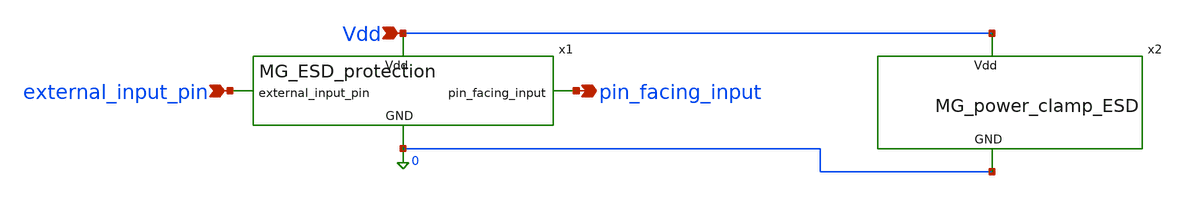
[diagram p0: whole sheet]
** sch_path: MG_ESD_protection/MG_ESD_protection_testbench.sch
**.subckt MG_ESD_protection_testbench external_input_pin Vdd pin_facing_input
*.ipin external_input_pin
*.ipin Vdd
*.opin pin_facing_input
x1 Vdd external_input_pin pin_facing_input 0 MG_ESD_protection
x2 Vdd 0 MG_power_clamp_ESD
**** begin user architecture code



.include /foss/pdks/gf180mcuD/libs.tech/ngspice/design.ngspice
.lib /foss/pdks/gf180mcuD/libs.tech/ngspice/sm141064.ngspice typical
.lib /foss/pdks/gf180mcuD/libs.tech/ngspice/sm141064.ngspice res_typical
.lib /foss/pdks/gf180mcuD/libs.tech/ngspice/sm141064.ngspice moscap_typical
.lib /foss/pdks/gf180mcuD/libs.tech/ngspice/sm141064.ngspice diode_typical
.lib /foss/pdks/gf180mcuD/libs.tech/ngspice/sm141064.ngspice mimcap_typical

* 1. Add ESD Current Source and Core Load Capacitor
* I_ESD injects the strike, and C_load represents the core receiver gate capacitance

I_ESD 0 external_input_pin PWL(0 0 1n 0)
C_load pin_facing_input 0 100f
Rleak Vdd 0 1G

* Add a controllable voltage source for Vdd (Assuming 3.3V - change to 5.0 if using 5V IOs)
* V_power Vdd 0 PWL(0 0)

.control

  * ==========================================
  * 3. HBM (Human Body Model) - 2kV Equivalent
  * Peak Current: ~1.33A, Rise: 5ns, Decay: ~150ns
  * ==========================================
  alter @I_ESD[pwl] = [ 0 0 5n 1.33 155n 0.49 305n 0.18 500n 0 ]



  * Run Transient Simulation (500ns duration, 1ns steps)
  tran 1n 1u

  * Extract Peak Voltages
  meas tran V_pad_max_HBM MAX v(external_input_pin)
  meas tran V_core_max_HBM MAX v(pin_facing_input)
  meas tran V_vdd_max_HBM MAX v(Vdd)

  * Print to Console
  print V_pad_max_HBM V_core_max_HBM


  * Plot HBM Waveforms
  plot v(external_input_pin) v(pin_facing_input) title 'HBM 2kV ESD Event' ylabel 'Voltage (V)' xlabel
+ 'Time (s)'
  plot v(pin_facing_input) title 'HBM 2kV ESD Event' ylabel 'Voltage (V)' xlabel 'Time (s)'
  plot v(Vdd) title 'HBM 2kV ESD Event' ylabel 'Vdd' xlabel 'Time'




* ==========================================
  * 3b. HBM - Power ON 1us after strike ends
  * Vdd ramps from 0V to 3.3V starting at 1.5us
  * ==========================================
*  alter @I_ESD[pwl] = [ 0 0 5n 1.33 155n 0.49 305n 0.18 500n 0 ]
*  alter @V_power[pwl] = [ 0 0 1.5u 0 1.6u 5 6u 5 ]

*  tran 0.1n 60u

*  meas tran V_pad_max_HBM_after MAX v(external_input_pin)
*  meas tran V_core_max_HBM_after MAX v(pin_facing_input)

*  print V_pad_max_HBM_after V_core_max_HBM_after
*  plot v(external_input_pin) v(pin_facing_input) title 'HBM (Power ON at 1.5us)' ylabel 'Voltage (V)'
*  plot v(Vdd) title 'HBM Vdd Supply (Delayed Power)' ylabel 'Vdd'

  * ==========================================
  * 3c. HBM - Powered ON during strike
  * Vdd is constant at 3.3V the entire time
  * ==========================================
*  alter @I_ESD[pwl] = [ 0 0 5n 1.33 155n 0.49 305n 0.18 500n 0 ]
*  alter @V_power[pwl] = [ 0 5 6u 5 ]

*  tran 0.1n 60u

*  meas tran V_pad_max_HBM_on MAX v(external_input_pin)
*  meas tran V_core_max_HBM_on MAX v(pin_facing_input)

*  print V_pad_max_HBM_on V_core_max_HBM_on
*  plot v(external_input_pin) v(pin_facing_input) title 'HBM (Already Powered ON)' ylabel 'Voltage (V)'

  * ==========================================
  * 4. CDM (Charged Device Model) - 500V Equivalent
  * Peak Current: ~5A, Rise: 250ps, Duration: ~2ns
  * ==========================================
  alter @I_ESD[pwl] = [ 0 0 250p 5.0 750p 0 1n -1.0 1.5n 0 3n 0 ]

  * Run Transient Simulation (3ns duration, 10ps steps)
  tran 10p 10n
  * Extract Peak Voltages
  meas tran V_pad_max_CDM MAX v(external_input_pin)
 meas tran V_core_max_CDM MAX v(pin_facing_input)
*  meas tran V_vdd_max_CDM MAX v(Vdd)

  * Print to Console
  print V_pad_max_CDM V_core_max_CDM


  * Plot CDM Waveforms
  plot v(external_input_pin) v(pin_facing_input) title 'CDM 500V ESD Event' ylabel 'Voltage (V)' xlabel
+ 'Time (s)'
  plot v(pin_facing_input) title 'CDM 500V ESD Event' ylabel 'Voltage (V)' xlabel 'Time (s)'
  plot v(Vdd) title 'CDM 500V ESD Event' ylabel 'Vdd' xlabel 'Time'

  * ==========================================
  * 4b. CDM - Power ON 1us after strike
  * Strike ends at 3ns. Vdd ramps to 3.3V starting at 1.003us
  * ==========================================
  * Reset V_power to default 0V before the run so earlier tests don't leak over
*  alter @V_power[pwl] = [ 0 0 1.003u 0 1.103u 5 6u 5 ]
*  alter @I_ESD[pwl] = [ 0 0 250p 5.0 750p 0 1n -1.0 1.5n 0 3n 0 ]

  * Note: 50p step used here to prevent massive file sizes over a 6us run
*  tran 50p 60u

*  meas tran V_pad_max_CDM_after MAX v(external_input_pin)
*  meas tran V_core_max_CDM_after MAX v(pin_facing_input)

*  print V_pad_max_CDM_after V_core_max_CDM_after
*  plot v(external_input_pin) v(pin_facing_input) title 'CDM (Power ON at 1us)' ylabel 'Voltage (V)'
*  plot v(Vdd) title 'CDM Vdd Supply (Delayed Power)' ylabel 'Vdd'

  * ==========================================
  * 4c. CDM - Powered ON during strike
  * Vdd is constant at 3.3V the entire time
  * ==========================================
*  alter @V_power[pwl] = [ 0 5 6u 5 ]
*  alter @I_ESD[pwl] = [ 0 0 250p 5.0 750p 0 1n -1.0 1.5n 0 3n 0 ]

*  tran 50p 60u

*  meas tran V_pad_max_CDM_on MAX v(external_input_pin)
*  meas tran V_core_max_CDM_on MAX v(pin_facing_input)

*  print V_pad_max_CDM_on V_core_max_CDM_on
*  plot v(external_input_pin) v(pin_facing_input) title 'CDM (Already Powered ON)' ylabel 'Voltage (V)'


.endc


**** end user architecture code
**.ends

* expanding   symbol:  MG_ESD_protection.sym # of pins=4
** sym_path: MG_ESD_protection/MG_ESD_protection.sym
** sch_path: MG_ESD_protection/MG_ESD_protection.sch
.subckt MG_ESD_protection Vdd external_input_pin pin_facing_input GND
*.ipin external_input_pin
*.ipin Vdd
*.ipin GND
*.opin pin_facing_input
D2 external_input_pin Vdd diode_pd2nw_06v0 area='25u * 0.9u ' pj='2*25u + 2*0.9u ' m=1
XR2 pin_facing_input external_input_pin GND ppolyf_u_1k_6p0 r_width=5e-6 r_length=10e-6 m=1
D1 GND external_input_pin diode_nd2ps_06v0 area='25u * 0.9u ' pj='2*25u + 2*0.9u ' m=1
D3 GND pin_facing_input diode_nd2ps_06v0 area='15u * 0.9u ' pj='2*15u + 2*0.9u ' m=1
D4 pin_facing_input Vdd diode_pd2nw_06v0 area='15u * 0.9u ' pj='2*15u + 2*0.9u ' m=1
D5 external_input_pin Vdd diode_pd2nw_06v0 area='25u * 0.9u ' pj='2*25u + 2*0.9u ' m=1
D6 GND external_input_pin diode_nd2ps_06v0 area='25u * 0.9u ' pj='2*25u + 2*0.9u ' m=1
D11 external_input_pin Vdd diode_pd2nw_06v0 area='25u * 0.9u ' pj='2*25u + 2*0.9u ' m=1
D12 GND external_input_pin diode_nd2ps_06v0 area='25u * 0.9u ' pj='2*25u + 2*0.9u ' m=1
D13 external_input_pin Vdd diode_pd2nw_06v0 area='25u * 0.9u ' pj='2*25u + 2*0.9u ' m=1
D14 GND external_input_pin diode_nd2ps_06v0 area='25u * 0.9u ' pj='2*25u + 2*0.9u ' m=1
D7 external_input_pin Vdd diode_pd2nw_06v0 area='25u * 0.9u ' pj='2*25u + 2*0.9u ' m=1
D8 GND external_input_pin diode_nd2ps_06v0 area='25u * 0.9u ' pj='2*25u + 2*0.9u ' m=1
D9 external_input_pin Vdd diode_pd2nw_06v0 area='25u * 0.9u ' pj='2*25u + 2*0.9u ' m=1
D10 GND external_input_pin diode_nd2ps_06v0 area='25u * 0.9u ' pj='2*25u + 2*0.9u ' m=1
.ends


* expanding   symbol:  MG_power_clamp_ESD.sym # of pins=2
** sym_path: MG_ESD_protection/MG_power_clamp_ESD.sym
** sch_path: MG_ESD_protection/MG_power_clamp_ESD.sch
.subckt MG_power_clamp_ESD Vdd GND
*.ipin Vdd
*.ipin GND
XC1 net1 GND cap_nmos_06v0 c_width=50e-6 c_length=50e-6 m=1
XMM_clamp3 Vdd clamp GND GND nfet_05v0 L=0.9u W=25u nf=1 ad='int((nf+1)/2) * W/nf * 0.18u' as='int((nf+2)/2)
+ * W/nf * 0.18u' pd='2*int((nf+1)/2) * (W/nf + 0.18u)' ps='2*int((nf+2)/2) * (W/nf + 0.18u)' nrd='0.18u
+ / W' nrs='0.18u / W' sa=0 sb=0 sd=0 m=1
XMM_clamp1 Vdd clamp GND GND nfet_05v0 L=0.9u W=25u nf=1 ad='int((nf+1)/2) * W/nf * 0.18u' as='int((nf+2)/2)
+ * W/nf * 0.18u' pd='2*int((nf+1)/2) * (W/nf + 0.18u)' ps='2*int((nf+2)/2) * (W/nf + 0.18u)' nrd='0.18u
+ / W' nrs='0.18u / W' sa=0 sb=0 sd=0 m=1
XMM_clamp2 Vdd clamp GND GND nfet_05v0 L=0.9u W=25u nf=1 ad='int((nf+1)/2) * W/nf * 0.18u' as='int((nf+2)/2)
+ * W/nf * 0.18u' pd='2*int((nf+1)/2) * (W/nf + 0.18u)' ps='2*int((nf+2)/2) * (W/nf + 0.18u)' nrd='0.18u
+ / W' nrs='0.18u / W' sa=0 sb=0 sd=0 m=1
XMM_clamp4 Vdd clamp GND GND nfet_05v0 L=0.9u W=25u nf=1 ad='int((nf+1)/2) * W/nf * 0.18u' as='int((nf+2)/2)
+ * W/nf * 0.18u' pd='2*int((nf+1)/2) * (W/nf + 0.18u)' ps='2*int((nf+2)/2) * (W/nf + 0.18u)' nrd='0.18u
+ / W' nrs='0.18u / W' sa=0 sb=0 sd=0 m=1
XMM_clamp5 Vdd clamp GND GND nfet_05v0 L=0.9u W=25u nf=1 ad='int((nf+1)/2) * W/nf * 0.18u' as='int((nf+2)/2)
+ * W/nf * 0.18u' pd='2*int((nf+1)/2) * (W/nf + 0.18u)' ps='2*int((nf+2)/2) * (W/nf + 0.18u)' nrd='0.18u
+ / W' nrs='0.18u / W' sa=0 sb=0 sd=0 m=1
XMM_clamp6 Vdd clamp GND GND nfet_05v0 L=0.9u W=25u nf=1 ad='int((nf+1)/2) * W/nf * 0.18u' as='int((nf+2)/2)
+ * W/nf * 0.18u' pd='2*int((nf+1)/2) * (W/nf + 0.18u)' ps='2*int((nf+2)/2) * (W/nf + 0.18u)' nrd='0.18u
+ / W' nrs='0.18u / W' sa=0 sb=0 sd=0 m=1
XMM_clamp7 Vdd clamp GND GND nfet_05v0 L=0.9u W=25u nf=1 ad='int((nf+1)/2) * W/nf * 0.18u' as='int((nf+2)/2)
+ * W/nf * 0.18u' pd='2*int((nf+1)/2) * (W/nf + 0.18u)' ps='2*int((nf+2)/2) * (W/nf + 0.18u)' nrd='0.18u
+ / W' nrs='0.18u / W' sa=0 sb=0 sd=0 m=1
XMM_clamp8 Vdd clamp GND GND nfet_05v0 L=0.9u W=25u nf=1 ad='int((nf+1)/2) * W/nf * 0.18u' as='int((nf+2)/2)
+ * W/nf * 0.18u' pd='2*int((nf+1)/2) * (W/nf + 0.18u)' ps='2*int((nf+2)/2) * (W/nf + 0.18u)' nrd='0.18u
+ / W' nrs='0.18u / W' sa=0 sb=0 sd=0 m=1
XMM_clamp9 Vdd clamp GND GND nfet_05v0 L=0.9u W=25u nf=1 ad='int((nf+1)/2) * W/nf * 0.18u' as='int((nf+2)/2)
+ * W/nf * 0.18u' pd='2*int((nf+1)/2) * (W/nf + 0.18u)' ps='2*int((nf+2)/2) * (W/nf + 0.18u)' nrd='0.18u
+ / W' nrs='0.18u / W' sa=0 sb=0 sd=0 m=1
XMM_clamp10 Vdd clamp GND GND nfet_05v0 L=0.9u W=25u nf=1 ad='int((nf+1)/2) * W/nf * 0.18u' as='int((nf+2)/2)
+ * W/nf * 0.18u' pd='2*int((nf+1)/2) * (W/nf + 0.18u)' ps='2*int((nf+2)/2) * (W/nf + 0.18u)' nrd='0.18u
+ / W' nrs='0.18u / W' sa=0 sb=0 sd=0 m=1
XMM_clamp11 Vdd clamp GND GND nfet_05v0 L=0.9u W=25u nf=1 ad='int((nf+1)/2) * W/nf * 0.18u' as='int((nf+2)/2)
+ * W/nf * 0.18u' pd='2*int((nf+1)/2) * (W/nf + 0.18u)' ps='2*int((nf+2)/2) * (W/nf + 0.18u)' nrd='0.18u
+ / W' nrs='0.18u / W' sa=0 sb=0 sd=0 m=1
XMM_clamp12 Vdd clamp GND GND nfet_05v0 L=0.9u W=25u nf=1 ad='int((nf+1)/2) * W/nf * 0.18u' as='int((nf+2)/2)
+ * W/nf * 0.18u' pd='2*int((nf+1)/2) * (W/nf + 0.18u)' ps='2*int((nf+2)/2) * (W/nf + 0.18u)' nrd='0.18u
+ / W' nrs='0.18u / W' sa=0 sb=0 sd=0 m=1
XR5 net2 net3 GND ppolyf_u_1k_6p0 r_width=2e-6 r_length=6e-5 m=1
XMM_clamp13 Vdd clamp GND GND nfet_05v0 L=0.9u W=25u nf=1 ad='int((nf+1)/2) * W/nf * 0.18u' as='int((nf+2)/2)
+ * W/nf * 0.18u' pd='2*int((nf+1)/2) * (W/nf + 0.18u)' ps='2*int((nf+2)/2) * (W/nf + 0.18u)' nrd='0.18u
+ / W' nrs='0.18u / W' sa=0 sb=0 sd=0 m=1
XMM_clamp14 Vdd clamp GND GND nfet_05v0 L=0.9u W=25u nf=1 ad='int((nf+1)/2) * W/nf * 0.18u' as='int((nf+2)/2)
+ * W/nf * 0.18u' pd='2*int((nf+1)/2) * (W/nf + 0.18u)' ps='2*int((nf+2)/2) * (W/nf + 0.18u)' nrd='0.18u
+ / W' nrs='0.18u / W' sa=0 sb=0 sd=0 m=1
XMM_clamp15 Vdd clamp GND GND nfet_05v0 L=0.9u W=25u nf=1 ad='int((nf+1)/2) * W/nf * 0.18u' as='int((nf+2)/2)
+ * W/nf * 0.18u' pd='2*int((nf+1)/2) * (W/nf + 0.18u)' ps='2*int((nf+2)/2) * (W/nf + 0.18u)' nrd='0.18u
+ / W' nrs='0.18u / W' sa=0 sb=0 sd=0 m=1
XMM_clamp16 Vdd clamp GND GND nfet_05v0 L=0.9u W=25u nf=1 ad='int((nf+1)/2) * W/nf * 0.18u' as='int((nf+2)/2)
+ * W/nf * 0.18u' pd='2*int((nf+1)/2) * (W/nf + 0.18u)' ps='2*int((nf+2)/2) * (W/nf + 0.18u)' nrd='0.18u
+ / W' nrs='0.18u / W' sa=0 sb=0 sd=0 m=1
XMM_clamp17 Vdd clamp GND GND nfet_05v0 L=0.9u W=25u nf=1 ad='int((nf+1)/2) * W/nf * 0.18u' as='int((nf+2)/2)
+ * W/nf * 0.18u' pd='2*int((nf+1)/2) * (W/nf + 0.18u)' ps='2*int((nf+2)/2) * (W/nf + 0.18u)' nrd='0.18u
+ / W' nrs='0.18u / W' sa=0 sb=0 sd=0 m=1
XMM_clamp18 Vdd clamp GND GND nfet_05v0 L=0.9u W=25u nf=1 ad='int((nf+1)/2) * W/nf * 0.18u' as='int((nf+2)/2)
+ * W/nf * 0.18u' pd='2*int((nf+1)/2) * (W/nf + 0.18u)' ps='2*int((nf+2)/2) * (W/nf + 0.18u)' nrd='0.18u
+ / W' nrs='0.18u / W' sa=0 sb=0 sd=0 m=1
XMM_clamp19 Vdd clamp GND GND nfet_05v0 L=0.9u W=25u nf=1 ad='int((nf+1)/2) * W/nf * 0.18u' as='int((nf+2)/2)
+ * W/nf * 0.18u' pd='2*int((nf+1)/2) * (W/nf + 0.18u)' ps='2*int((nf+2)/2) * (W/nf + 0.18u)' nrd='0.18u
+ / W' nrs='0.18u / W' sa=0 sb=0 sd=0 m=1
XMM_clamp20 Vdd clamp GND GND nfet_05v0 L=0.9u W=25u nf=1 ad='int((nf+1)/2) * W/nf * 0.18u' as='int((nf+2)/2)
+ * W/nf * 0.18u' pd='2*int((nf+1)/2) * (W/nf + 0.18u)' ps='2*int((nf+2)/2) * (W/nf + 0.18u)' nrd='0.18u
+ / W' nrs='0.18u / W' sa=0 sb=0 sd=0 m=1
XMM_clamp21 Vdd clamp GND GND nfet_05v0 L=0.9u W=25u nf=1 ad='int((nf+1)/2) * W/nf * 0.18u' as='int((nf+2)/2)
+ * W/nf * 0.18u' pd='2*int((nf+1)/2) * (W/nf + 0.18u)' ps='2*int((nf+2)/2) * (W/nf + 0.18u)' nrd='0.18u
+ / W' nrs='0.18u / W' sa=0 sb=0 sd=0 m=1
XMM_clamp22 Vdd clamp GND GND nfet_05v0 L=0.9u W=25u nf=1 ad='int((nf+1)/2) * W/nf * 0.18u' as='int((nf+2)/2)
+ * W/nf * 0.18u' pd='2*int((nf+1)/2) * (W/nf + 0.18u)' ps='2*int((nf+2)/2) * (W/nf + 0.18u)' nrd='0.18u
+ / W' nrs='0.18u / W' sa=0 sb=0 sd=0 m=1
XMM_clamp23 Vdd clamp GND GND nfet_05v0 L=0.9u W=25u nf=1 ad='int((nf+1)/2) * W/nf * 0.18u' as='int((nf+2)/2)
+ * W/nf * 0.18u' pd='2*int((nf+1)/2) * (W/nf + 0.18u)' ps='2*int((nf+2)/2) * (W/nf + 0.18u)' nrd='0.18u
+ / W' nrs='0.18u / W' sa=0 sb=0 sd=0 m=1
XMM_clamp24 Vdd clamp GND GND nfet_05v0 L=0.9u W=25u nf=1 ad='int((nf+1)/2) * W/nf * 0.18u' as='int((nf+2)/2)
+ * W/nf * 0.18u' pd='2*int((nf+1)/2) * (W/nf + 0.18u)' ps='2*int((nf+2)/2) * (W/nf + 0.18u)' nrd='0.18u
+ / W' nrs='0.18u / W' sa=0 sb=0 sd=0 m=1
XMM_p2 clamp net1 Vdd Vdd pfet_05v0 L=0.9u W=60u nf=10 ad='int((nf+1)/2) * W/nf * 0.18u' as='int((nf+2)/2)
+ * W/nf * 0.18u' pd='2*int((nf+1)/2) * (W/nf + 0.18u)' ps='2*int((nf+2)/2) * (W/nf + 0.18u)' nrd='0.18u
+ / W' nrs='0.18u / W' sa=0 sb=0 sd=0 m=1
XMM_n2 clamp net1 GND GND nfet_05v0 L=0.9u W=24u nf=4 ad='int((nf+1)/2) * W/nf * 0.18u' as='int((nf+2)/2)
+ * W/nf * 0.18u' pd='2*int((nf+1)/2) * (W/nf + 0.18u)' ps='2*int((nf+2)/2) * (W/nf + 0.18u)' nrd='0.18u
+ / W' nrs='0.18u / W' sa=0 sb=0 sd=0 m=1
XR1 net4 net1 GND ppolyf_u_1k_6p0 r_width=2e-6 r_length=6e-5 m=1
XR2 net5 net4 GND ppolyf_u_1k_6p0 r_width=2e-6 r_length=6e-5 m=1
XR3 net6 net5 GND ppolyf_u_1k_6p0 r_width=2e-6 r_length=6e-5 m=1
XR4 net3 net6 GND ppolyf_u_1k_6p0 r_width=2e-6 r_length=6e-5 m=1
XR6 net7 net2 GND ppolyf_u_1k_6p0 r_width=2e-6 r_length=6e-5 m=1
XR7 net8 net7 GND ppolyf_u_1k_6p0 r_width=2e-6 r_length=6e-5 m=1
XR8 Vdd net8 GND ppolyf_u_1k_6p0 r_width=2e-6 r_length=6e-5 m=1
XMM_clamp25 Vdd clamp GND GND nfet_05v0 L=0.9u W=25u nf=1 ad='int((nf+1)/2) * W/nf * 0.18u' as='int((nf+2)/2)
+ * W/nf * 0.18u' pd='2*int((nf+1)/2) * (W/nf + 0.18u)' ps='2*int((nf+2)/2) * (W/nf + 0.18u)' nrd='0.18u
+ / W' nrs='0.18u / W' sa=0 sb=0 sd=0 m=1
XMM_clamp26 Vdd clamp GND GND nfet_05v0 L=0.9u W=25u nf=1 ad='int((nf+1)/2) * W/nf * 0.18u' as='int((nf+2)/2)
+ * W/nf * 0.18u' pd='2*int((nf+1)/2) * (W/nf + 0.18u)' ps='2*int((nf+2)/2) * (W/nf + 0.18u)' nrd='0.18u
+ / W' nrs='0.18u / W' sa=0 sb=0 sd=0 m=1
.ends

.end
